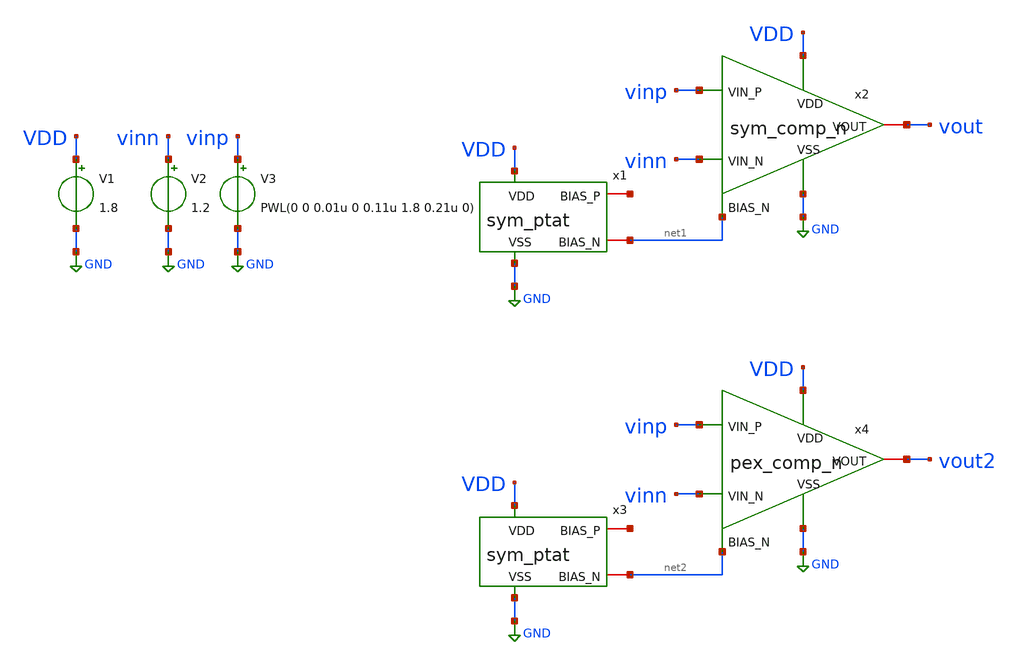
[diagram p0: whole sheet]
** sch_path: schem/tb/tb_comp_n.sch
**.subckt tb_comp_n
V1 VDD GND 1.8
V2 vinn GND 1.2
V3 vinp GND PWL(0 0 0.01u 0 0.11u 1.8 0.21u 0)
x1 VDD GND net3 net1 sym_ptat
x2 VDD GND vinn vinp vout net1 sym_comp_n
x3 VDD GND net4 net2 sym_ptat
x4 VDD GND vinn vinp vout2 net2 comp_n
**** begin user architecture code


.include /home/zhixuan/projects/fyp_vco/magic/ip/comp_n/comp_n.spice
.lib /usr/local/share/pdk/sky130A/libs.tech/ngspice/sky130.lib.spice tt

.tran 0.1n 0.21u
.save all

.control
    run
    plot vinn vinp vout vout2

   echo "vinn vinp vout2" > /home/zhixuan/projects/fyp_vco/schem/tb/compn_tb_out1.txt
   print col vinn vinp vout2 >> /home/zhixuan/projects/fyp_vco/schem/tb/compn_tb_out1.txt
.endc

.end


**** end user architecture code
**.ends

* expanding   symbol:  /home/zhixuan/projects/fyp_vco/schem/symbol_repo/sym_ptat.sym # of pins=4
** sym_path: schem/symbol_repo/sym_ptat.sym
** sch_path: schem/symbol_repo/sym_ptat.sch
.subckt sym_ptat VDD VSS BIAS_P BIAS_N
*.ipin VDD
*.ipin VSS
*.iopin BIAS_P
*.iopin BIAS_N
XMN_ptat2 net6 net1 net2 VSS sky130_fd_pr__nfet_01v8 L=0.5 W=2 nf=2 ad='int((2 + 1)/2) * 2 / 2 * 0.29'
+ as='int((2 + 2)/2) * 2 / 2 * 0.29' pd='2*int((2 + 1)/2) * (2 / 2 + 0.29)' ps='2*int((2 + 2)/2) * (2 / 2 + 0.29)'
+ nrd='0.29 / 2 ' nrs='0.29 / 2 ' sa=0 sb=0 sd=0 mult=1 m=1
XMP_diode1 net3 BIAS_P VDD VDD sky130_fd_pr__pfet_01v8 L=0.5 W=2 nf=2 ad='int((2 + 1)/2) * 2 / 2 * 0.29'
+ as='int((2 + 2)/2) * 2 / 2 * 0.29' pd='2*int((2 + 1)/2) * (2 / 2 + 0.29)' ps='2*int((2 + 2)/2) * (2 / 2 + 0.29)'
+ nrd='0.29 / 2 ' nrs='0.29 / 2 ' sa=0 sb=0 sd=0 mult=1 m=1
XMP_mir1_l net4 BIAS_P VDD VDD sky130_fd_pr__pfet_01v8 L=0.5 W=2 nf=2 ad='int((2 + 1)/2) * 2 / 2 * 0.29'
+ as='int((2 + 2)/2) * 2 / 2 * 0.29' pd='2*int((2 + 1)/2) * (2 / 2 + 0.29)' ps='2*int((2 + 2)/2) * (2 / 2 + 0.29)'
+ nrd='0.29 / 2 ' nrs='0.29 / 2 ' sa=0 sb=0 sd=0 mult=1 m=1
XMN_diode2 net5 net1 VSS VSS sky130_fd_pr__nfet_01v8 L=0.5 W=2 nf=4 ad='int((4 + 1)/2) * 2 / 4 * 0.29'
+ as='int((4 + 2)/2) * 2 / 4 * 0.29' pd='2*int((4 + 1)/2) * (2 / 4 + 0.29)' ps='2*int((4 + 2)/2) * (2 / 4 + 0.29)'
+ nrd='0.29 / 2 ' nrs='0.29 / 2 ' sa=0 sb=0 sd=0 mult=1 m=1
XMP_inv BIAS_N BIAS_P VDD VDD sky130_fd_pr__pfet_01v8 L=0.75 W=2 nf=5 ad='int((5 + 1)/2) * 2 / 5 * 0.29'
+ as='int((5 + 2)/2) * 2 / 5 * 0.29' pd='2*int((5 + 1)/2) * (2 / 5 + 0.29)' ps='2*int((5 + 2)/2) * (2 / 5 + 0.29)'
+ nrd='0.29 / 2 ' nrs='0.29 / 2 ' sa=0 sb=0 sd=0 mult=1 m=1
XMP_diode2 BIAS_P BIAS_P net3 VDD sky130_fd_pr__pfet_01v8 L=0.5 W=2 nf=2 ad='int((2 + 1)/2) * 2 / 2 * 0.29'
+ as='int((2 + 2)/2) * 2 / 2 * 0.29' pd='2*int((2 + 1)/2) * (2 / 2 + 0.29)' ps='2*int((2 + 2)/2) * (2 / 2 + 0.29)'
+ nrd='0.29 / 2 ' nrs='0.29 / 2 ' sa=0 sb=0 sd=0 mult=1 m=1
XMP_mir2_l net1 BIAS_P net4 VDD sky130_fd_pr__pfet_01v8 L=0.5 W=2 nf=2 ad='int((2 + 1)/2) * 2 / 2 * 0.29'
+ as='int((2 + 2)/2) * 2 / 2 * 0.29' pd='2*int((2 + 1)/2) * (2 / 2 + 0.29)' ps='2*int((2 + 2)/2) * (2 / 2 + 0.29)'
+ nrd='0.29 / 2 ' nrs='0.29 / 2 ' sa=0 sb=0 sd=0 mult=1 m=1
XMN_ptat1 BIAS_P net1 net6 VSS sky130_fd_pr__nfet_01v8 L=0.5 W=2 nf=2 ad='int((2 + 1)/2) * 2 / 2 * 0.29'
+ as='int((2 + 2)/2) * 2 / 2 * 0.29' pd='2*int((2 + 1)/2) * (2 / 2 + 0.29)' ps='2*int((2 + 2)/2) * (2 / 2 + 0.29)'
+ nrd='0.29 / 2 ' nrs='0.29 / 2 ' sa=0 sb=0 sd=0 mult=1 m=1
XMN_diode1 net1 net1 net5 VSS sky130_fd_pr__nfet_01v8 L=0.5 W=2 nf=4 ad='int((4 + 1)/2) * 2 / 4 * 0.29'
+ as='int((4 + 2)/2) * 2 / 4 * 0.29' pd='2*int((4 + 1)/2) * (2 / 4 + 0.29)' ps='2*int((4 + 2)/2) * (2 / 4 + 0.29)'
+ nrd='0.29 / 2 ' nrs='0.29 / 2 ' sa=0 sb=0 sd=0 mult=1 m=1
XMN_inv BIAS_N BIAS_N VSS VSS sky130_fd_pr__nfet_01v8 L=0.75 W=2.5 nf=2 ad='int((2 + 1)/2) * 2.5 / 2 * 0.29'
+ as='int((2 + 2)/2) * 2.5 / 2 * 0.29' pd='2*int((2 + 1)/2) * (2.5 / 2 + 0.29)' ps='2*int((2 + 2)/2) * (2.5 / 2 + 0.29)'
+ nrd='0.29 / 2.5 ' nrs='0.29 / 2.5 ' sa=0 sb=0 sd=0 mult=1 m=1
XR1 VSS net2 VSS sky130_fd_pr__res_xhigh_po_0p35 L=2.8 mult=1 m=1
XMP_startup net1 VSS VDD VDD sky130_fd_pr__pfet_01v8 L=13 W=1 nf=1 ad='int((1 + 1)/2) * 1 / 1 * 0.29'
+ as='int((1 + 2)/2) * 1 / 1 * 0.29' pd='2*int((1 + 1)/2) * (1 / 1 + 0.29)' ps='2*int((1 + 2)/2) * (1 / 1 + 0.29)'
+ nrd='0.29 / 1 ' nrs='0.29 / 1 ' sa=0 sb=0 sd=0 mult=1 m=1
XMN_diode3 net7 net1 VSS VSS sky130_fd_pr__nfet_01v8 L=0.5 W=2 nf=4 ad='int((4 + 1)/2) * 2 / 4 * 0.29'
+ as='int((4 + 2)/2) * 2 / 4 * 0.29' pd='2*int((4 + 1)/2) * (2 / 4 + 0.29)' ps='2*int((4 + 2)/2) * (2 / 4 + 0.29)'
+ nrd='0.29 / 2 ' nrs='0.29 / 2 ' sa=0 sb=0 sd=0 mult=1 m=1
XMN_diode4 net1 net1 net7 VSS sky130_fd_pr__nfet_01v8 L=0.5 W=2 nf=4 ad='int((4 + 1)/2) * 2 / 4 * 0.29'
+ as='int((4 + 2)/2) * 2 / 4 * 0.29' pd='2*int((4 + 1)/2) * (2 / 4 + 0.29)' ps='2*int((4 + 2)/2) * (2 / 4 + 0.29)'
+ nrd='0.29 / 2 ' nrs='0.29 / 2 ' sa=0 sb=0 sd=0 mult=1 m=1
.ends


* expanding   symbol:  /home/zhixuan/projects/fyp_vco/schem/symbol_repo/sym_comp_n.sym # of pins=6
** sym_path: schem/symbol_repo/sym_comp_n.sym
** sch_path: schem/symbol_repo/sym_comp_n.sch
.subckt sym_comp_n VDD VSS VIN_N VIN_P VOUT BIAS_N
*.ipin VDD
*.ipin VSS
*.ipin VIN_N
*.ipin VIN_P
*.ipin BIAS_N
*.iopin VOUT
XMP_diode_l net1 net1 VDD VDD sky130_fd_pr__pfet_01v8 L=0.3 W=2 nf=2 ad='int((2 + 1)/2) * 2 / 2 * 0.29'
+ as='int((2 + 2)/2) * 2 / 2 * 0.29' pd='2*int((2 + 1)/2) * (2 / 2 + 0.29)' ps='2*int((2 + 2)/2) * (2 / 2 + 0.29)'
+ nrd='0.29 / 2 ' nrs='0.29 / 2 ' sa=0 sb=0 sd=0 mult=1 m=1
XMP_cs_l net2 net1 VDD VDD sky130_fd_pr__pfet_01v8 L=0.3 W=2 nf=2 ad='int((2 + 1)/2) * 2 / 2 * 0.29'
+ as='int((2 + 2)/2) * 2 / 2 * 0.29' pd='2*int((2 + 1)/2) * (2 / 2 + 0.29)' ps='2*int((2 + 2)/2) * (2 / 2 + 0.29)'
+ nrd='0.29 / 2 ' nrs='0.29 / 2 ' sa=0 sb=0 sd=0 mult=1 m=1
XMP_cs_r net1 net2 VDD VDD sky130_fd_pr__pfet_01v8 L=0.3 W=2 nf=2 ad='int((2 + 1)/2) * 2 / 2 * 0.29'
+ as='int((2 + 2)/2) * 2 / 2 * 0.29' pd='2*int((2 + 1)/2) * (2 / 2 + 0.29)' ps='2*int((2 + 2)/2) * (2 / 2 + 0.29)'
+ nrd='0.29 / 2 ' nrs='0.29 / 2 ' sa=0 sb=0 sd=0 mult=1 m=1
XMP_diode_r net2 net2 VDD VDD sky130_fd_pr__pfet_01v8 L=0.3 W=2 nf=2 ad='int((2 + 1)/2) * 2 / 2 * 0.29'
+ as='int((2 + 2)/2) * 2 / 2 * 0.29' pd='2*int((2 + 1)/2) * (2 / 2 + 0.29)' ps='2*int((2 + 2)/2) * (2 / 2 + 0.29)'
+ nrd='0.29 / 2 ' nrs='0.29 / 2 ' sa=0 sb=0 sd=0 mult=1 m=1
XMN_vinn net1 VIN_N net3 VSS sky130_fd_pr__nfet_01v8 L=0.5 W=2.5 nf=1 ad='int((1 + 1)/2) * 2.5 / 1 * 0.29'
+ as='int((1 + 2)/2) * 2.5 / 1 * 0.29' pd='2*int((1 + 1)/2) * (2.5 / 1 + 0.29)' ps='2*int((1 + 2)/2) * (2.5 / 1 + 0.29)'
+ nrd='0.29 / 2.5 ' nrs='0.29 / 2.5 ' sa=0 sb=0 sd=0 mult=1 m=1
XMN_vinp net2 VIN_P net3 VSS sky130_fd_pr__nfet_01v8 L=0.5 W=2.5 nf=1 ad='int((1 + 1)/2) * 2.5 / 1 * 0.29'
+ as='int((1 + 2)/2) * 2.5 / 1 * 0.29' pd='2*int((1 + 1)/2) * (2.5 / 1 + 0.29)' ps='2*int((1 + 2)/2) * (2.5 / 1 + 0.29)'
+ nrd='0.29 / 2.5 ' nrs='0.29 / 2.5 ' sa=0 sb=0 sd=0 mult=1 m=1
XMN_tail net3 BIAS_N VSS VSS sky130_fd_pr__nfet_01v8 L=0.75 W=2.5 nf=2 ad='int((2 + 1)/2) * 2.5 / 2 * 0.29'
+ as='int((2 + 2)/2) * 2.5 / 2 * 0.29' pd='2*int((2 + 1)/2) * (2.5 / 2 + 0.29)' ps='2*int((2 + 2)/2) * (2.5 / 2 + 0.29)'
+ nrd='0.29 / 2.5 ' nrs='0.29 / 2.5 ' sa=0 sb=0 sd=0 mult=1 m=1
XMP_latch_r VOUT net2 VDD VDD sky130_fd_pr__pfet_01v8 L=0.15 W=0.5 nf=1 ad='int((1 + 1)/2) * 0.5 / 1 * 0.29'
+ as='int((1 + 2)/2) * 0.5 / 1 * 0.29' pd='2*int((1 + 1)/2) * (0.5 / 1 + 0.29)' ps='2*int((1 + 2)/2) * (0.5 / 1 + 0.29)'
+ nrd='0.29 / 0.5 ' nrs='0.29 / 0.5 ' sa=0 sb=0 sd=0 mult=1 m=1
XMP_latch_l net5 net1 VDD VDD sky130_fd_pr__pfet_01v8 L=0.15 W=0.5 nf=1 ad='int((1 + 1)/2) * 0.5 / 1 * 0.29'
+ as='int((1 + 2)/2) * 0.5 / 1 * 0.29' pd='2*int((1 + 1)/2) * (0.5 / 1 + 0.29)' ps='2*int((1 + 2)/2) * (0.5 / 1 + 0.29)'
+ nrd='0.29 / 0.5 ' nrs='0.29 / 0.5 ' sa=0 sb=0 sd=0 mult=1 m=1
XMN_latch_r VOUT net4 VSS VSS sky130_fd_pr__nfet_01v8 L=0.15 W=0.5 nf=1 ad='int((1 + 1)/2) * 0.5 / 1 * 0.29'
+ as='int((1 + 2)/2) * 0.5 / 1 * 0.29' pd='2*int((1 + 1)/2) * (0.5 / 1 + 0.29)' ps='2*int((1 + 2)/2) * (0.5 / 1 + 0.29)'
+ nrd='0.29 / 0.5 ' nrs='0.29 / 0.5 ' sa=0 sb=0 sd=0 mult=1 m=1
XMN_diode_l net4 net4 VSS VSS sky130_fd_pr__nfet_01v8 L=0.15 W=0.5 nf=1 ad='int((1 + 1)/2) * 0.5 / 1 * 0.29'
+ as='int((1 + 2)/2) * 0.5 / 1 * 0.29' pd='2*int((1 + 1)/2) * (0.5 / 1 + 0.29)' ps='2*int((1 + 2)/2) * (0.5 / 1 + 0.29)'
+ nrd='0.29 / 0.5 ' nrs='0.29 / 0.5 ' sa=0 sb=0 sd=0 mult=1 m=1
XMP_lim net4 net4 net5 VDD sky130_fd_pr__pfet_01v8 L=0.15 W=0.5 nf=1 ad='int((1 + 1)/2) * 0.5 / 1 * 0.29'
+ as='int((1 + 2)/2) * 0.5 / 1 * 0.29' pd='2*int((1 + 1)/2) * (0.5 / 1 + 0.29)' ps='2*int((1 + 2)/2) * (0.5 / 1 + 0.29)'
+ nrd='0.29 / 0.5 ' nrs='0.29 / 0.5 ' sa=0 sb=0 sd=0 mult=1 m=1
.ends

.GLOBAL GND
.end
